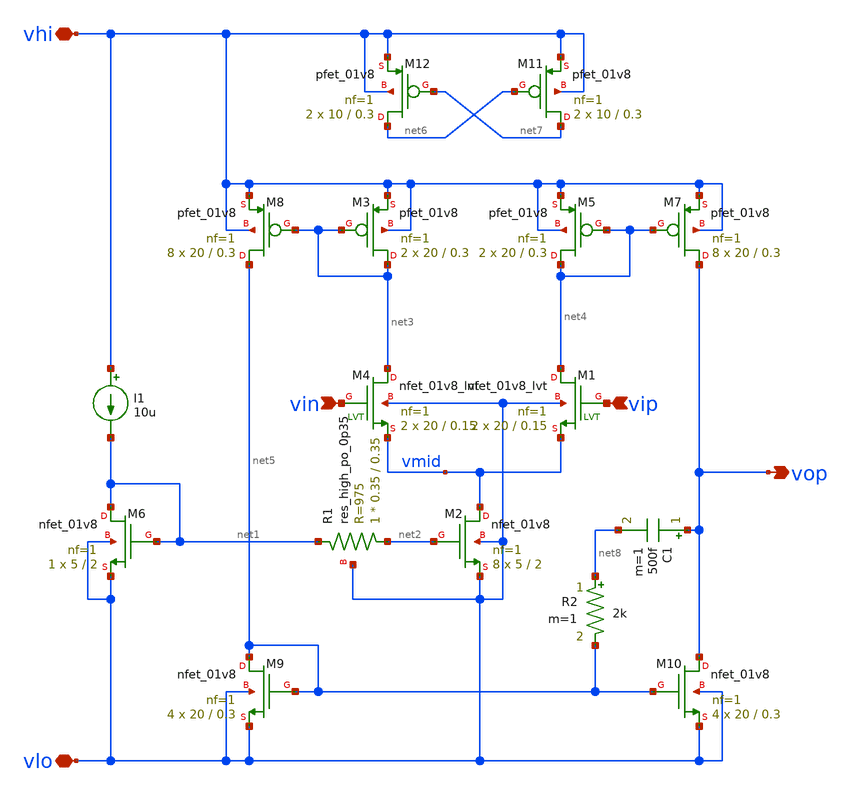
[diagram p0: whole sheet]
** sch_path: xschem/i_type_ota_model.sch
**.subckt i_type_ota_model vip vin vop vhi vlo
*.ipin vip
*.ipin vin
*.opin vop
*.iopin vhi
*.iopin vlo
XM2 vmid net2 vlo vlo sky130_fd_pr__nfet_01v8 L=2 W=5 nf=1 ad='int((nf+1)/2) * W/nf * 0.29' as='int((nf+2)/2) * W/nf * 0.29'
+ pd='2*int((nf+1)/2) * (W/nf + 0.29)' ps='2*int((nf+2)/2) * (W/nf + 0.29)' nrd='0.29 / W' nrs='0.29 / W'
+ sa=0 sb=0 sd=0 mult=8 m=8
XM6 net1 net1 vlo vlo sky130_fd_pr__nfet_01v8 L=2 W=5 nf=1 ad='int((nf+1)/2) * W/nf * 0.29' as='int((nf+2)/2) * W/nf * 0.29'
+ pd='2*int((nf+1)/2) * (W/nf + 0.29)' ps='2*int((nf+2)/2) * (W/nf + 0.29)' nrd='0.29 / W' nrs='0.29 / W'
+ sa=0 sb=0 sd=0 mult=1 m=1
I1 vhi net1 10u
XR1 net2 net1 vlo sky130_fd_pr__res_high_po_0p35 L=0.35 mult=1 m=1
XM4 net3 vin vmid vlo sky130_fd_pr__nfet_01v8_lvt L=0.15 W=20 nf=1 ad='int((nf+1)/2) * W/nf * 0.29' as='int((nf+2)/2) * W/nf * 0.29'
+ pd='2*int((nf+1)/2) * (W/nf + 0.29)' ps='2*int((nf+2)/2) * (W/nf + 0.29)' nrd='0.29 / W' nrs='0.29 / W'
+ sa=0 sb=0 sd=0 mult=2 m=2
XM1 net4 vip vmid vlo sky130_fd_pr__nfet_01v8_lvt L=0.15 W=20 nf=1 ad='int((nf+1)/2) * W/nf * 0.29' as='int((nf+2)/2) * W/nf * 0.29'
+ pd='2*int((nf+1)/2) * (W/nf + 0.29)' ps='2*int((nf+2)/2) * (W/nf + 0.29)' nrd='0.29 / W' nrs='0.29 / W'
+ sa=0 sb=0 sd=0 mult=2 m=2
XM3 net3 net3 vhi vhi sky130_fd_pr__pfet_01v8 L=0.3 W=20 nf=1 ad='int((nf+1)/2) * W/nf * 0.29' as='int((nf+2)/2) * W/nf * 0.29'
+ pd='2*int((nf+1)/2) * (W/nf + 0.29)' ps='2*int((nf+2)/2) * (W/nf + 0.29)' nrd='0.29 / W' nrs='0.29 / W'
+ sa=0 sb=0 sd=0 mult=2 m=2
XM5 net4 net4 vhi vhi sky130_fd_pr__pfet_01v8 L=0.3 W=20 nf=1 ad='int((nf+1)/2) * W/nf * 0.29' as='int((nf+2)/2) * W/nf * 0.29'
+ pd='2*int((nf+1)/2) * (W/nf + 0.29)' ps='2*int((nf+2)/2) * (W/nf + 0.29)' nrd='0.29 / W' nrs='0.29 / W'
+ sa=0 sb=0 sd=0 mult=2 m=2
XM7 vop net4 vhi vhi sky130_fd_pr__pfet_01v8 L=0.3 W=20 nf=1 ad='int((nf+1)/2) * W/nf * 0.29' as='int((nf+2)/2) * W/nf * 0.29'
+ pd='2*int((nf+1)/2) * (W/nf + 0.29)' ps='2*int((nf+2)/2) * (W/nf + 0.29)' nrd='0.29 / W' nrs='0.29 / W'
+ sa=0 sb=0 sd=0 mult=8 m=8
XM8 net5 net3 vhi vhi sky130_fd_pr__pfet_01v8 L=0.3 W=20 nf=1 ad='int((nf+1)/2) * W/nf * 0.29' as='int((nf+2)/2) * W/nf * 0.29'
+ pd='2*int((nf+1)/2) * (W/nf + 0.29)' ps='2*int((nf+2)/2) * (W/nf + 0.29)' nrd='0.29 / W' nrs='0.29 / W'
+ sa=0 sb=0 sd=0 mult=8 m=8
XM9 net5 net5 vlo vlo sky130_fd_pr__nfet_01v8 L=0.3 W=20 nf=1 ad='int((nf+1)/2) * W/nf * 0.29' as='int((nf+2)/2) * W/nf * 0.29'
+ pd='2*int((nf+1)/2) * (W/nf + 0.29)' ps='2*int((nf+2)/2) * (W/nf + 0.29)' nrd='0.29 / W' nrs='0.29 / W'
+ sa=0 sb=0 sd=0 mult=4 m=4
XM10 vop net5 vlo vlo sky130_fd_pr__nfet_01v8 L=0.3 W=20 nf=1 ad='int((nf+1)/2) * W/nf * 0.29' as='int((nf+2)/2) * W/nf * 0.29'
+ pd='2*int((nf+1)/2) * (W/nf + 0.29)' ps='2*int((nf+2)/2) * (W/nf + 0.29)' nrd='0.29 / W' nrs='0.29 / W'
+ sa=0 sb=0 sd=0 mult=4 m=4
XM11 net7 net6 vhi vhi sky130_fd_pr__pfet_01v8 L=0.3 W=10 nf=1 ad='int((nf+1)/2) * W/nf * 0.29' as='int((nf+2)/2) * W/nf * 0.29'
+ pd='2*int((nf+1)/2) * (W/nf + 0.29)' ps='2*int((nf+2)/2) * (W/nf + 0.29)' nrd='0.29 / W' nrs='0.29 / W'
+ sa=0 sb=0 sd=0 mult=2 m=2
XM12 net6 net7 vhi vhi sky130_fd_pr__pfet_01v8 L=0.3 W=10 nf=1 ad='int((nf+1)/2) * W/nf * 0.29' as='int((nf+2)/2) * W/nf * 0.29'
+ pd='2*int((nf+1)/2) * (W/nf + 0.29)' ps='2*int((nf+2)/2) * (W/nf + 0.29)' nrd='0.29 / W' nrs='0.29 / W'
+ sa=0 sb=0 sd=0 mult=2 m=2
C1 vop net8 500f m=1
R2 net8 net5 2k m=1
**.ends
.end
